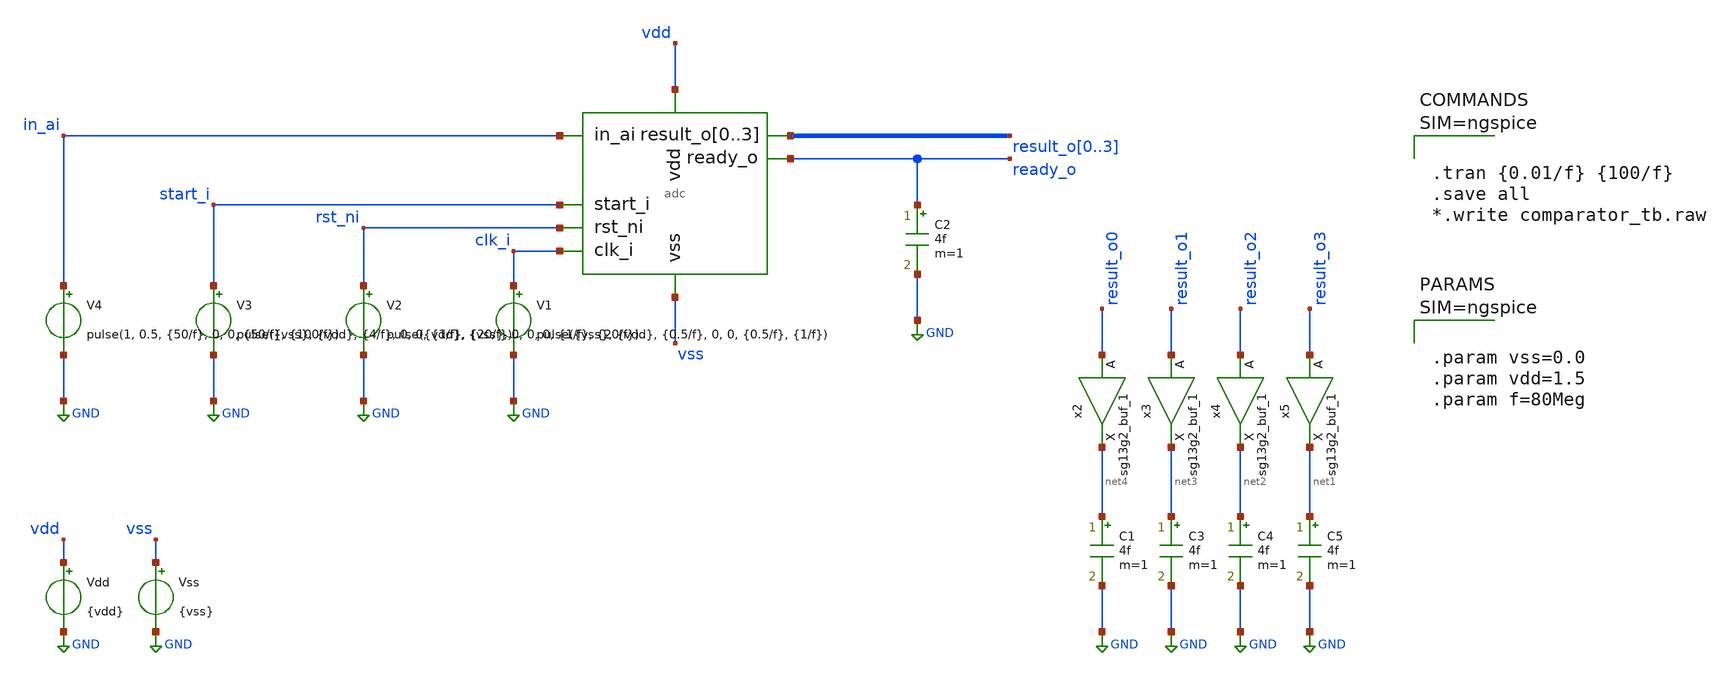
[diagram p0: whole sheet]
** sch_path: designs/basic/adc_tb.sch
* IHP-GmbH/IHP-Open-PDK/ihp-sg13g2/libs.tech/xschem/sg13g2_stdcells/sg13g2_buf_1.sch:
* Copyright 2023 IHP PDK Authors
* Licensed under the Apache License, Version 2.0 (the "License");
**.subckt adc_tb
x1 in_ai start_i rst_ni clk_i result_o0 result_o1 result_o2 result_o3 ready_o vdd vss adc
V1 clk_i GND pulse({vss}, {vdd}, {0.5/f}, 0, 0, {0.5/f}, {1/f})
V2 rst_ni GND pulse({vdd}, {vss}, 0, 0, 0, {1/f}, {20/f})
V3 start_i GND pulse({vss}, {vdd}, {4/f}, 0, 0, {1/f}, {20/f})
V4 in_ai GND pulse(1, 0.5, {50/f}, 0, 0, {50/f}, {100/f})
.save i(v4)
Vdd vdd GND {vdd}
Vss vss GND {vss}
C1 net4 GND 4f m=1
C2 ready_o GND 4f m=1
C3 net3 GND 4f m=1
C4 net2 GND 4f m=1
C5 net1 GND 4f m=1
x2 net4 result_o0 VDD VSS sg13g2_buf_1
x3 net3 result_o1 VDD VSS sg13g2_buf_1
x4 net2 result_o2 VDD VSS sg13g2_buf_1
x5 net1 result_o3 VDD VSS sg13g2_buf_1
**** begin user architecture code

.lib $::SG13G2_MODELS/cornerMOSlv.lib mos_tt
.lib $::SG13G2_MODELS/cornerCAP.lib cap_typ
.include $::PDK_ROOT/ihp-sg13g2/libs.ref/sg13g2_stdcell/spice/sg13g2_stdcell.spice




.tran {0.01/f} {100/f}
.save all
*.write comparator_tb.raw






.param vss=0.0
.param vdd=1.5
.param f=80Meg






.model adc_buff_clk adc_bridge(in_low = 'vdd/2' in_high = 'vdd/2')

.control
pre_set auto_bridge_d_out =  ( ".model auto_bridge_out bidi_bridge(direction=0 out_high=1.5
+ t_rise=1n t_fall=1n)"    "auto_bridge_out%d [ %s ] [ %s ] null auto_bridge_out" )
pre_set auto_bridge_d_in =  ( ".model auto_bridge_in bidi_bridge(direction=1 in_low=0.5 in_high=1)"
+    "auto_bridge_in%d [ %s ] [ %s ] null auto_bridge_in" )
.endc



**** end user architecture code
**.ends

* expanding   symbol:  adc.sym # of pins=8
** sym_path: designs/basic/adc.sym
** sch_path: designs/basic/adc.sch
.subckt adc in_ai start_i rst_ni clk_i result_o0 result_o1 result_o2 result_o3 ready_o vdd vss
*.ipin in_ai
*.ipin clk_i
*.ipin vss
*.ipin vdd
*.ipin rst_ni
*.ipin start_i
*.opin ready_o
*.opin result_o0,result_o1,result_o2,result_o3
x2 net3 sample vss net4 net1 vss vdd net5 comparator
x3 sample result_o0 result_o1 result_o2 result_o3 result_o0 result_o1 result_o2 result_o3 vss vdd
+ cdac
x4 clk_n clk_i VDD VSS sg13g2_inv_1
* noconn #net4
x5 comp net6 clk_n net1 rst_ni VDD VSS sg13g2_dfrbp_1
* noconn #net6
A2 [ clk_i ] [ net2 ] adc_buff_clk
x7 rst_i rst_ni VDD VSS sg13g2_inv_1
A1 [ net2 start_i rst_ni comp ] [ ready_o sample_o result_o0 result_o1 result_o2 result_o3 ] adc
.ends


* expanding   symbol:  sg13g2_stdcells/sg13g2_buf_1.sym # of pins=2
** sym_path: sg13g2_stdcells/sg13g2_buf_1.sym
** sch_path: sg13g2_stdcells/sg13g2_buf_1.sch
.subckt sg13g2_buf_1 X A VDD VSS
*.ipin A
*.opin X
*.iopin VDD
*.iopin VSS
XM1 net1 A VSS VSS sg13_lv_nmos w=550.00n l=130.00n ng=1 m=1 mm_ok=1
XM2 X net1 VSS VSS sg13_lv_nmos w=740.00n l=130.00n ng=1 m=1 mm_ok=1
XM3 net1 A VDD VDD sg13_lv_pmos w=840.00n l=130.00n ng=1 m=1 mm_ok=1
XM4 X net1 VDD VDD sg13_lv_pmos w=1.12u l=130.00n ng=1 m=1 mm_ok=1
.ends


* expanding   symbol:  /workspaces/ngspice_cosim_inv/designs/comparator/comparator.sym # of pins=8
** sym_path: designs/comparator_dt/comparator.sym
** sch_path: designs/comparator_dt/comparator.sch
.subckt comparator clk_i pos_ai neg_ai neg_o pos_o VSS VDD clk_ni
*.ipin pos_ai
*.ipin neg_ai
*.ipin VSS
*.ipin VDD
*.opin neg_o
*.opin pos_o
*.ipin clk_i
*.ipin clk_ni
XM12 neg_buf clk_i VDD VDD sg13_lv_pmos w=1.0u l=0.13u ng=1 m=1 mm_ok=1
XM13 pos_buf clk_i VDD VDD sg13_lv_pmos w=1.0u l=0.13u ng=1 m=1 mm_ok=1
XM14 net1 pos_ai neg_buf VSS sg13_lv_nmos w=1.0u l=0.13u ng=1 m=1 mm_ok=1
XM15 net1 neg_ai pos_buf VSS sg13_lv_nmos w=1.0u l=0.13u ng=1 m=1 mm_ok=1
XM16 VSS clk_i net1 VSS sg13_lv_nmos w=1.0u l=0.13u ng=1 m=1 mm_ok=1
XM17 net2 clk_ni VDD VDD sg13_lv_pmos w=2.0u l=0.13u ng=2 m=1 mm_ok=1
XM18 pos_o neg_o net2 VDD sg13_lv_pmos w=2.0u l=0.13u ng=2 m=1 mm_ok=1
XM19 neg_o pos_o net2 VDD sg13_lv_pmos w=2.0u l=0.13u ng=2 m=1 mm_ok=1
XM20 VSS neg_buf pos_o VSS sg13_lv_nmos w=1.0u l=0.13u ng=1 m=1 mm_ok=1
XM21 VSS neg_o pos_o VSS sg13_lv_nmos w=1.0u l=0.13u ng=1 m=1 mm_ok=1
XM22 VSS pos_o neg_o VSS sg13_lv_nmos w=1.0u l=0.13u ng=1 m=1 mm_ok=1
XM23 VSS pos_buf neg_o VSS sg13_lv_nmos w=1.0u l=0.13u ng=1 m=1 mm_ok=1
XC1 neg_buf VSS cap_cmim w=1.41e-5 l=1.41e-5 m=1 mm_ok=1
XC2 pos_buf VSS cap_cmim w=1.41e-5 l=1.41e-5 m=1 mm_ok=1
.ends


* expanding   symbol:  /workspaces/ngspice_cosim_inv/designs/cdac/cdac.sym # of pins=4
** sym_path: designs/cdac/cdac.sym
** sch_path: designs/cdac/cdac.sch
.subckt cdac VIN CTRL0 CTRL1 CTRL2 CTRL3 CTRL4 CTRL5 CTRL6 CTRL7 VSS VDD
*.ipin VIN
*.ipin CTRL0,CTRL1,CTRL2,CTRL3,CTRL4,CTRL5,CTRL6,CTRL7
*.ipin VSS
*.ipin VDD
XC2 VIN l1 cap_cmim w=7.297e-5 l=7.298e-5 m=1 mm_ok=1
XC3 VIN l2 cap_cmim w=5.158e-5 l=5.159e-5 m=1 mm_ok=1
XC4 VIN l3 cap_cmim w=3.646e-5 l=3.646e-5 m=1 mm_ok=1
XC5 VIN VSS cap_cmim w=6.402e-6 l=6.402e-6 m=1 mm_ok=1
x1 l1 CTRL0 VDD VSS sg13g2_inv_2
x2 l2 CTRL1 VDD VSS sg13g2_inv_2
x3 l3 CTRL2 VDD VSS sg13g2_inv_2
x4 l4 CTRL3 VDD VSS sg13g2_inv_2
XC6 VIN l4 cap_cmim w=2.577e-5 l=2.577e-5 m=1 mm_ok=1
XC7 VIN l5 cap_cmim w=1.820e-5 l=1.820e-5 m=1 mm_ok=1
XC8 VIN l6 cap_cmim w=1.286e-5 l=1.286e-5 m=1 mm_ok=1
XC9 VIN l7 cap_cmim w=9.077e-6 l=9.077e-6 m=1 mm_ok=1
x5 l5 CTRL4 VDD VSS sg13g2_inv_2
x6 l6 CTRL5 VDD VSS sg13g2_inv_2
x7 l7 CTRL6 VDD VSS sg13g2_inv_2
x8 l8 CTRL7 VDD VSS sg13g2_inv_2
XC1 VIN l8 cap_cmim w=6.402e-6 l=6.402e-6 m=1 mm_ok=1
.ends


* expanding   symbol:  sg13g2_stdcells/sg13g2_inv_1.sym # of pins=2
** sym_path: sg13g2_stdcells/sg13g2_inv_1.sym
** sch_path: sg13g2_stdcells/sg13g2_inv_1.sch
.subckt sg13g2_inv_1 Y A VDD VSS
*.opin Y
*.ipin A
*.iopin VDD
*.iopin VSS
XM1 Y A VSS VSS sg13_lv_nmos w=740.00n l=130.00n ng=1 m=1 mm_ok=1
XM2 Y A VDD VDD sg13_lv_pmos w=1.12u l=130.00n ng=1 m=1 mm_ok=1
.ends


* expanding   symbol:  sg13g2_stdcells/sg13g2_dfrbp_1.sym # of pins=5
** sym_path: sg13g2_stdcells/sg13g2_dfrbp_1.sym
** sch_path: sg13g2_stdcells/sg13g2_dfrbp_1.sch
.subckt sg13g2_dfrbp_1 Q Q_N CLK D RESET_B VDD VSS
*.ipin D
*.ipin RESET_B
*.ipin CLK
*.opin Q
*.opin Q_N
*.iopin VDD
*.iopin VSS
XM1 Db D net10 VSS sg13_lv_nmos w=420.00n l=130.00n ng=1 m=1 mm_ok=1
XM2 net10 RESET_B VSS VSS sg13_lv_nmos w=420.00n l=130.00n ng=1 m=1 mm_ok=1
XM3 net1 clkneg net9 VSS sg13_lv_nmos w=420.00n l=130.00n ng=1 m=1 mm_ok=1
XM4 net9 net1 VSS VSS sg13_lv_nmos w=420.00n l=130.00n ng=1 m=1 mm_ok=1
XM5 net1 net1 net5 VSS sg13_lv_nmos w=420.00n l=130.00n ng=1 m=1 mm_ok=1
XM6 net5 RESET_B VSS VSS sg13_lv_nmos w=420.00n l=130.00n ng=1 m=1 mm_ok=1
XM7 Q_N net1 VSS VSS sg13_lv_nmos w=740.00n l=130.00n ng=1 m=1 mm_ok=1
XM8 net2 net1 VSS VSS sg13_lv_nmos w=740.00n l=130.00n ng=1 m=1 mm_ok=1
XM9 Q net2 VSS VSS sg13_lv_nmos w=740.00n l=130.00n ng=1 m=1 mm_ok=1
XM10 clkneg CLK VSS VSS sg13_lv_nmos w=740.00n l=130.00n ng=1 m=1 mm_ok=1
XM11 clkpos clkneg VSS VSS sg13_lv_nmos w=740.00n l=130.00n ng=1 m=1 mm_ok=1
XM12 Db clkneg net3 VSS sg13_lv_nmos w=420.00n l=130.00n ng=1 m=1 mm_ok=1
XM13 net3 clkpos net8 VSS sg13_lv_nmos w=420.00n l=130.00n ng=1 m=1 mm_ok=1
XM14 net8 net3 net4 VSS sg13_lv_nmos w=420.00n l=130.00n ng=1 m=1 mm_ok=1
XM15 net4 RESET_B VSS VSS sg13_lv_nmos w=420.00n l=130.00n ng=1 m=1 mm_ok=1
XM16 net3 net3 VSS VSS sg13_lv_nmos w=740.00n l=130.00n ng=1 m=1 mm_ok=1
XM17 net3 clkpos net1 VSS sg13_lv_nmos w=740.00n l=130.00n ng=1 m=1 mm_ok=1
XM18 Db RESET_B VDD VDD sg13_lv_pmos w=420.00n l=130.00n ng=1 m=1 mm_ok=1
XM19 Db D VDD VDD sg13_lv_pmos w=420.00n l=130.00n ng=1 m=1 mm_ok=1
XM20 net7 net1 VDD VDD sg13_lv_pmos w=420.00n l=130.00n ng=1 m=1 mm_ok=1
XM21 net1 clkpos net7 VDD sg13_lv_pmos w=420.00n l=130.00n ng=1 m=1 mm_ok=1
XM22 net1 net1 VDD VDD sg13_lv_pmos w=420.00n l=130.00n ng=1 m=1 mm_ok=1
XM23 net1 RESET_B VDD VDD sg13_lv_pmos w=420.00n l=130.00n ng=1 m=1 mm_ok=1
XM24 Q_N net1 VDD VDD sg13_lv_pmos w=1.12u l=130.00n ng=1 m=1 mm_ok=1
XM25 net2 net1 VDD VDD sg13_lv_pmos w=1.12u l=130.00n ng=1 m=1 mm_ok=1
XM26 Q net2 VDD VDD sg13_lv_pmos w=1.12u l=130.00n ng=1 m=1 mm_ok=1
XM27 clkneg CLK VDD VDD sg13_lv_pmos w=1.12u l=130.00n ng=1 m=1 mm_ok=1
XM28 clkpos clkneg VDD VDD sg13_lv_pmos w=1.12u l=130.00n ng=1 m=1 mm_ok=1
XM29 Db clkpos net3 VDD sg13_lv_pmos w=420.00n l=130.00n ng=1 m=1 mm_ok=1
XM30 net6 net3 VDD VDD sg13_lv_pmos w=420.00n l=130.00n ng=1 m=1 mm_ok=1
XM31 net3 clkneg net6 VDD sg13_lv_pmos w=420.00n l=130.00n ng=1 m=1 mm_ok=1
XM32 net3 RESET_B VDD VDD sg13_lv_pmos w=420.00n l=130.00n ng=1 m=1 mm_ok=1
XM33 net3 net3 VDD VDD sg13_lv_pmos w=1.000u l=130.00n ng=1 m=1 mm_ok=1
XM34 net3 clkneg net1 VDD sg13_lv_pmos w=1.000u l=130.00n ng=1 m=1 mm_ok=1
.ends


* expanding   symbol:  sg13g2_stdcells/sg13g2_inv_2.sym # of pins=2
** sym_path: sg13g2_stdcells/sg13g2_inv_2.sym
** sch_path: sg13g2_stdcells/sg13g2_inv_2.sch
.subckt sg13g2_inv_2 Y A VDD VSS
*.opin Y
*.ipin A
*.iopin VDD
*.iopin VSS
XM1 Y A VSS VSS sg13_lv_nmos w=1.48u l=130.00n ng=2 m=1 mm_ok=1
XM2 Y A VDD VDD sg13_lv_pmos w=2.24u l=130.00n ng=2 m=1 mm_ok=1
.ends

.GLOBAL GND
**** begin user architecture code
.model adc d_cosim simulation="ivlng" sim_args=["adc"]
**** end user architecture code
.end
